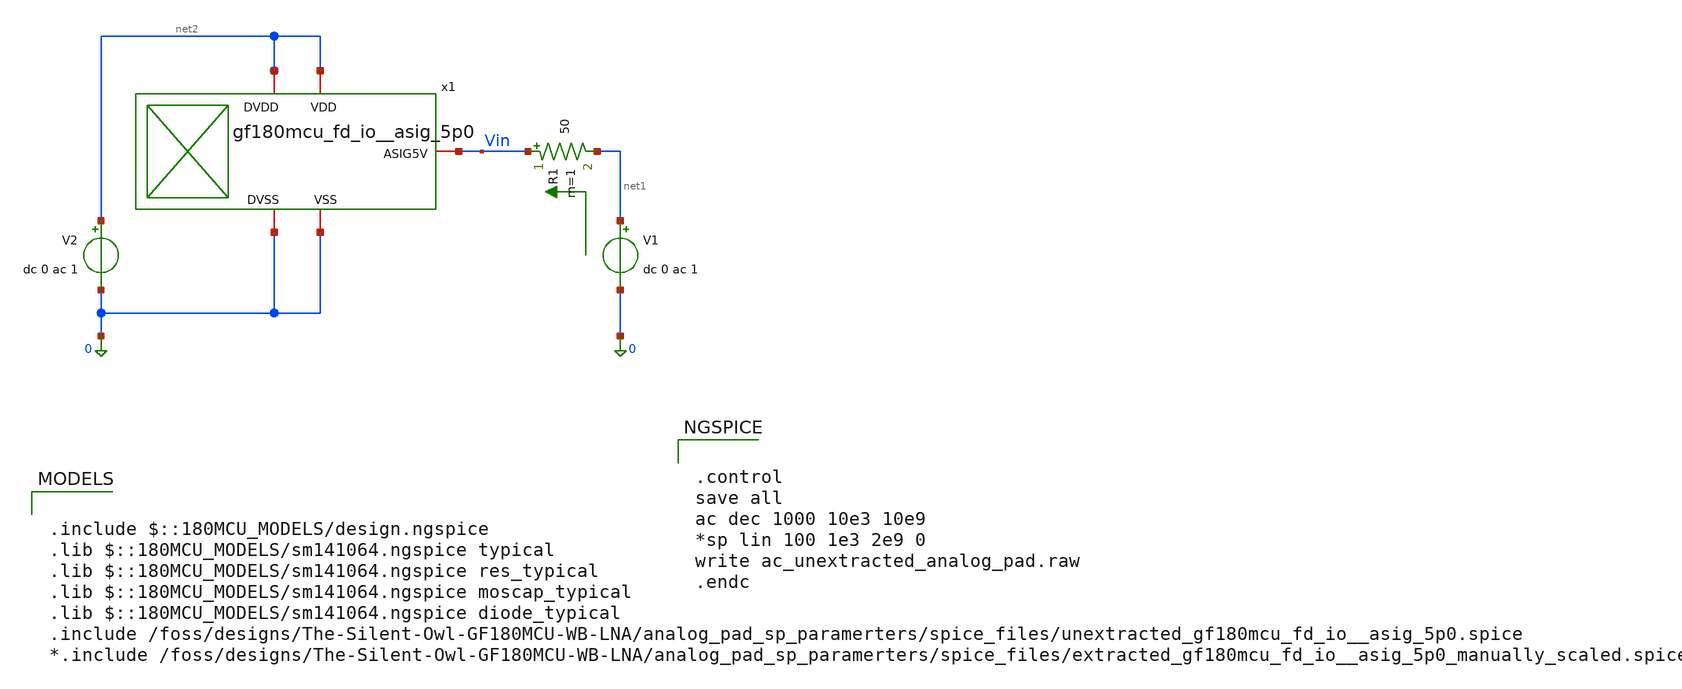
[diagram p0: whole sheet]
** sch_path: analog_pad_sp_paramerters/xschem/schematic_unextracted_ac.sch
**.subckt schematic_unextracted_ac
V1 net1 0 dc 0 ac 1
R1 Vin net1 50 m=1
x1 Vin net2 0 net2 0 gf180mcu_fd_io__asig_5p0
V2 net2 0 dc 0 ac 1
**** begin user architecture code


.control
save all
ac dec 1000 10e3 10e9
*sp lin 100 1e3 2e9 0
write ac_unextracted_analog_pad.raw
.endc



.include $::180MCU_MODELS/design.ngspice
.lib $::180MCU_MODELS/sm141064.ngspice typical
.lib $::180MCU_MODELS/sm141064.ngspice res_typical
.lib $::180MCU_MODELS/sm141064.ngspice moscap_typical
.lib $::180MCU_MODELS/sm141064.ngspice diode_typical
.include /foss/designs/The-Silent-Owl-GF180MCU-WB-LNA/analog_pad_sp_paramerters/spice_files/unextracted_gf180mcu_fd_io__asig_5p0.spice
*.include /foss/designs/The-Silent-Owl-GF180MCU-WB-LNA/analog_pad_sp_paramerters/spice_files/extracted_gf180mcu_fd_io__asig_5p0_manually_scaled.spice

**** end user architecture code
**.ends
.end
